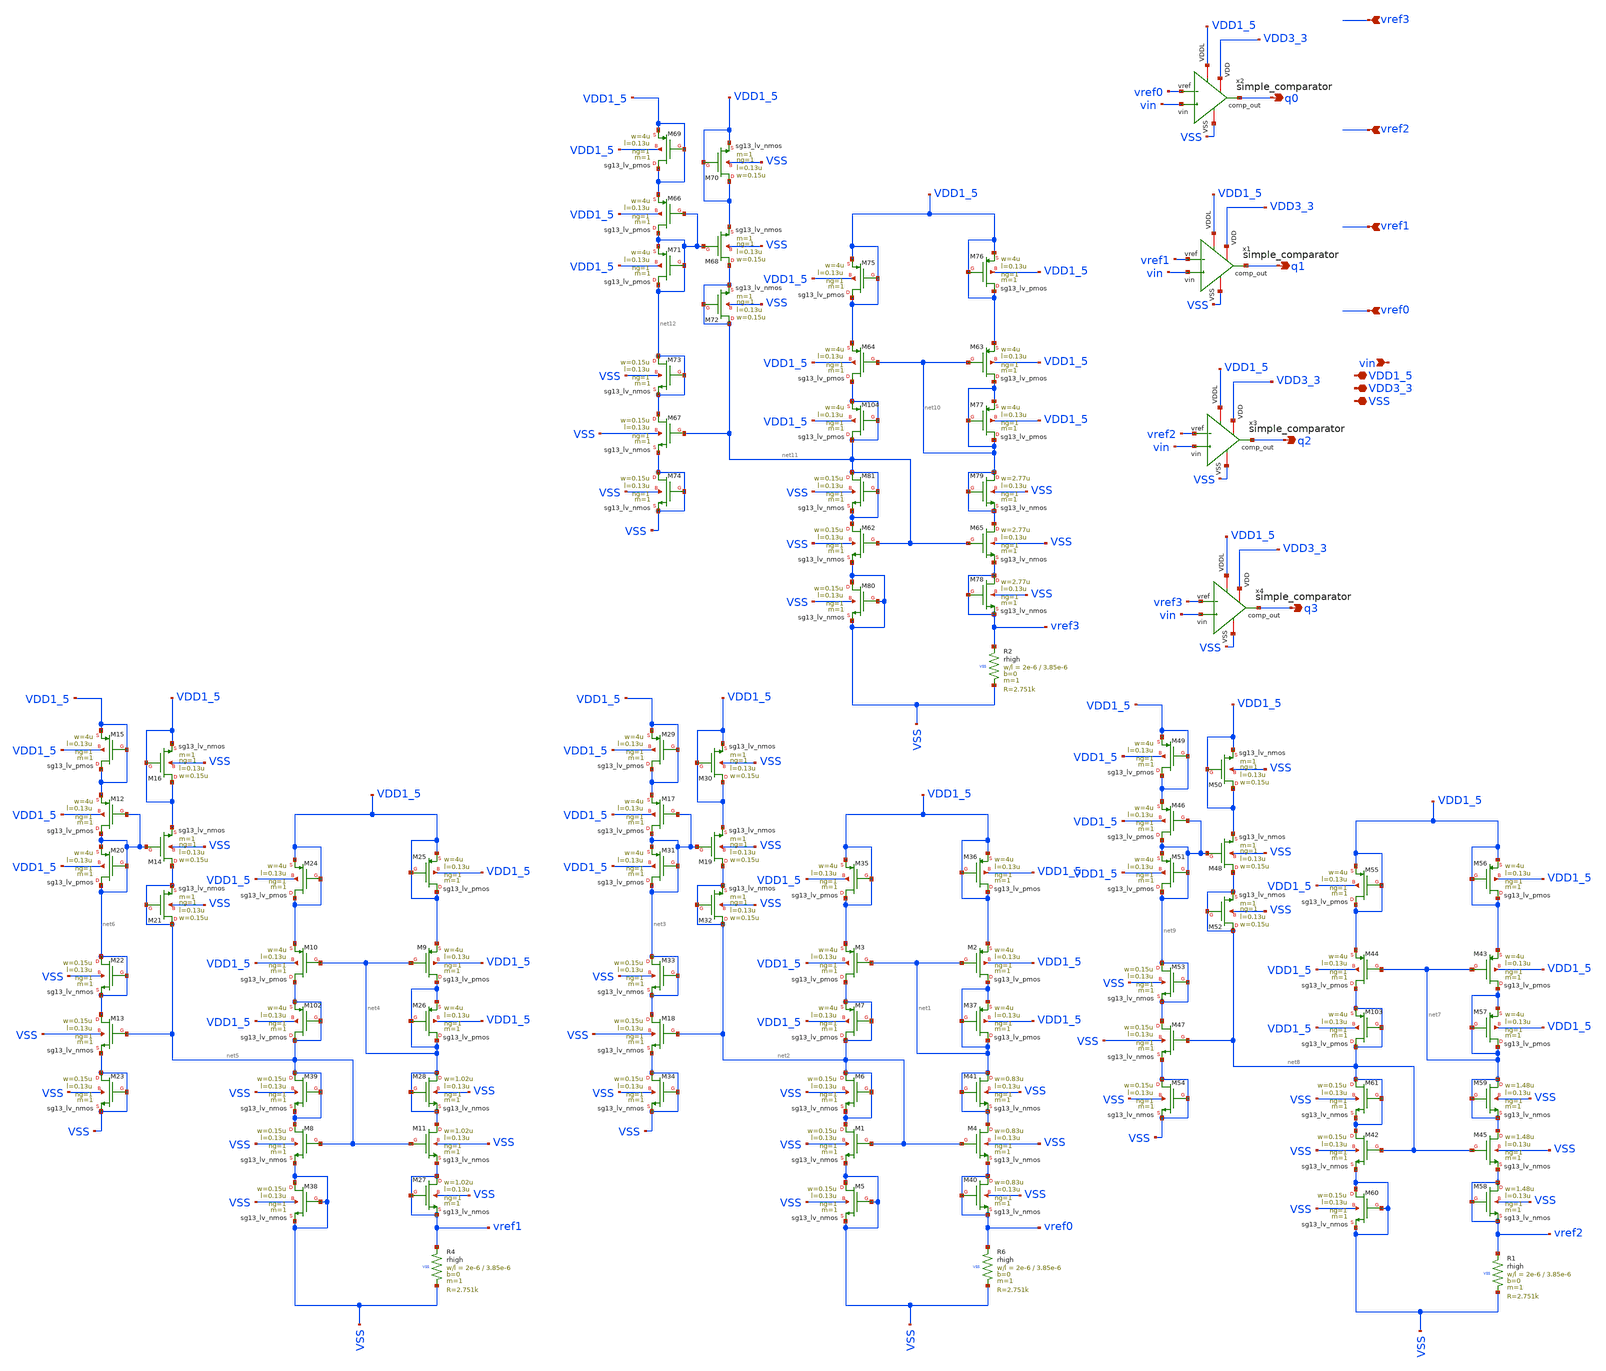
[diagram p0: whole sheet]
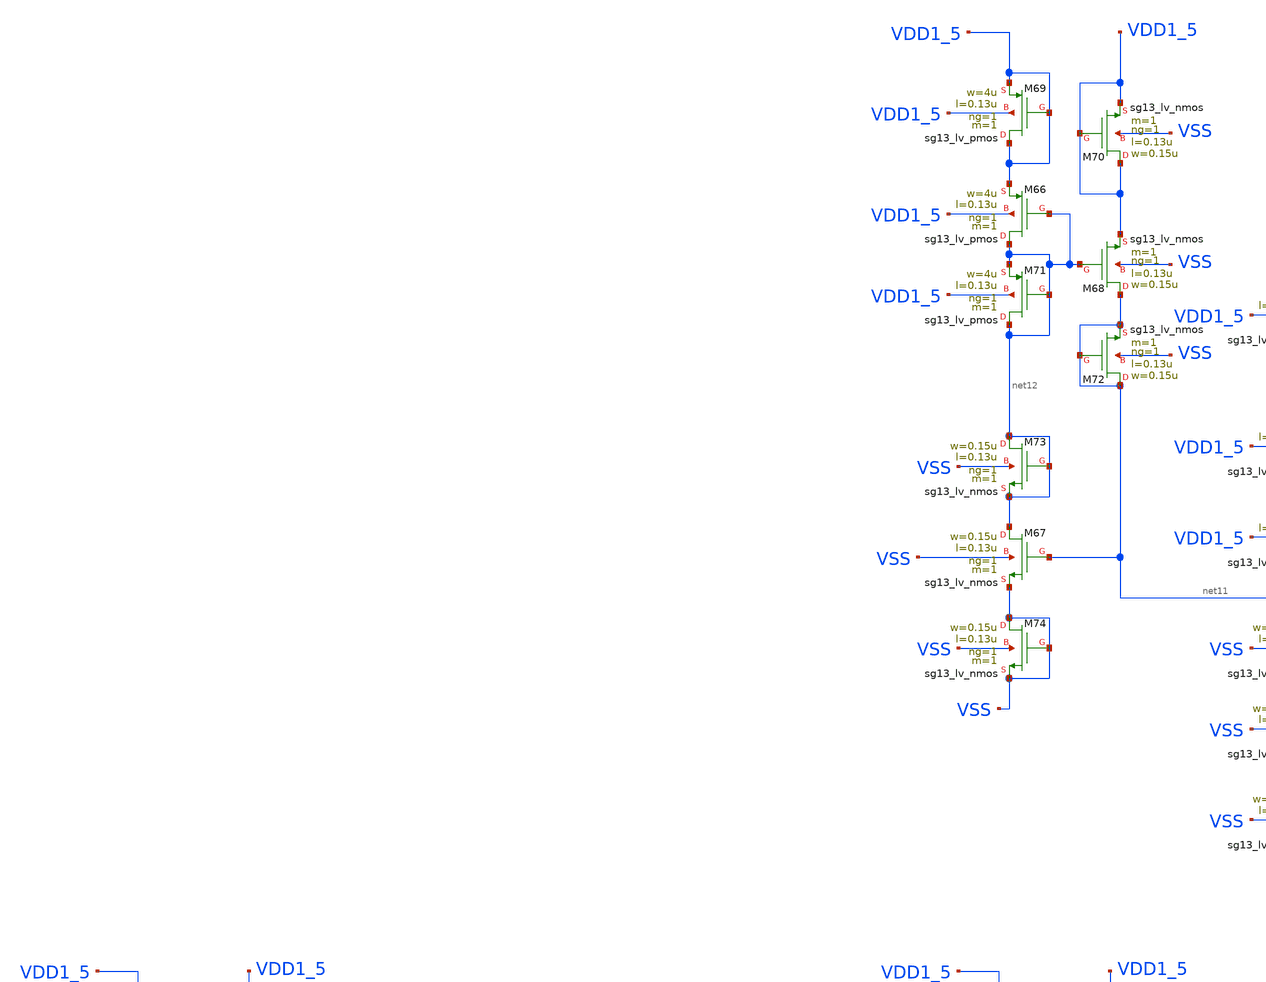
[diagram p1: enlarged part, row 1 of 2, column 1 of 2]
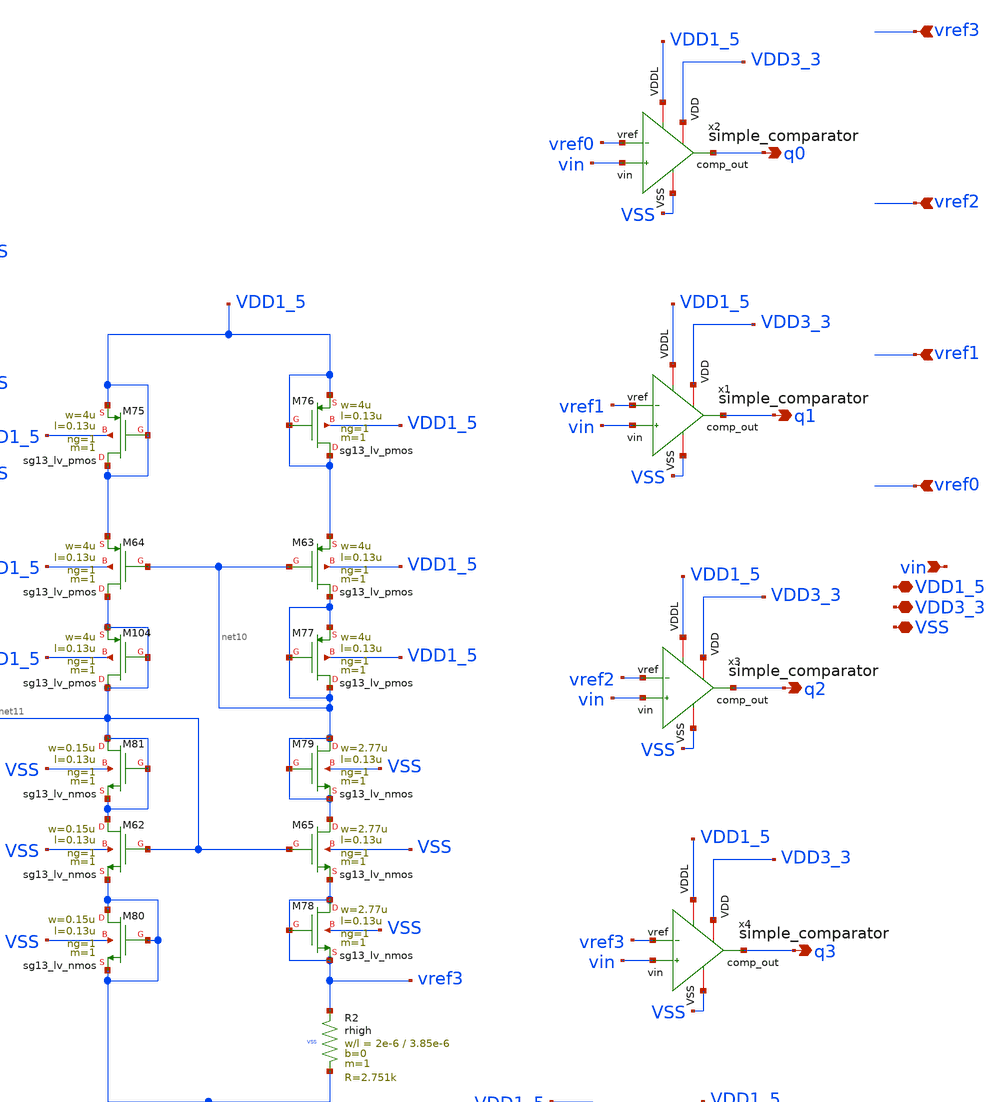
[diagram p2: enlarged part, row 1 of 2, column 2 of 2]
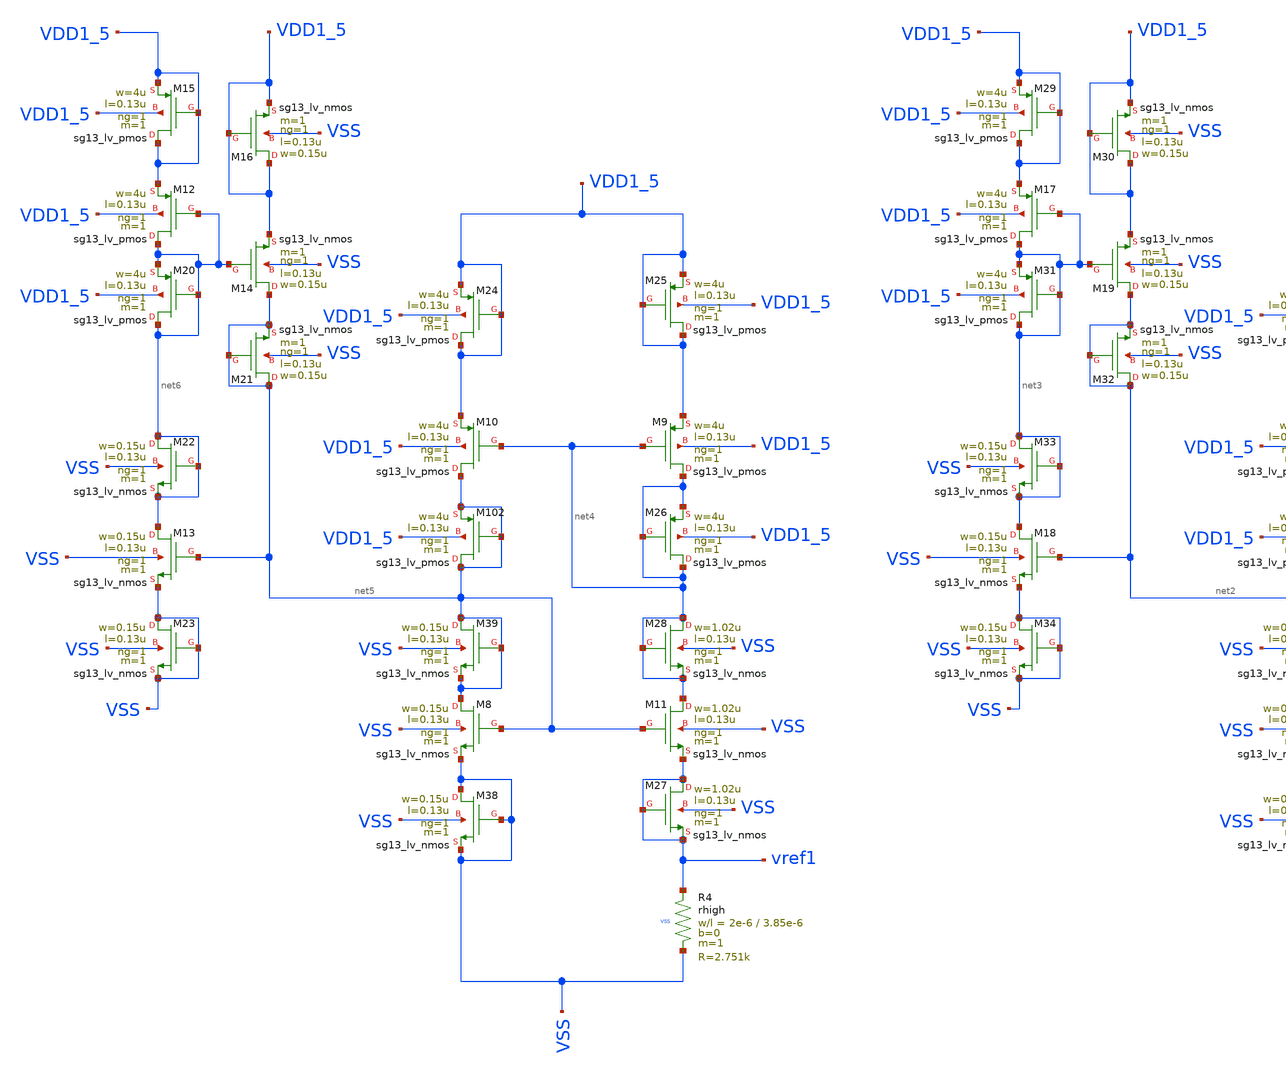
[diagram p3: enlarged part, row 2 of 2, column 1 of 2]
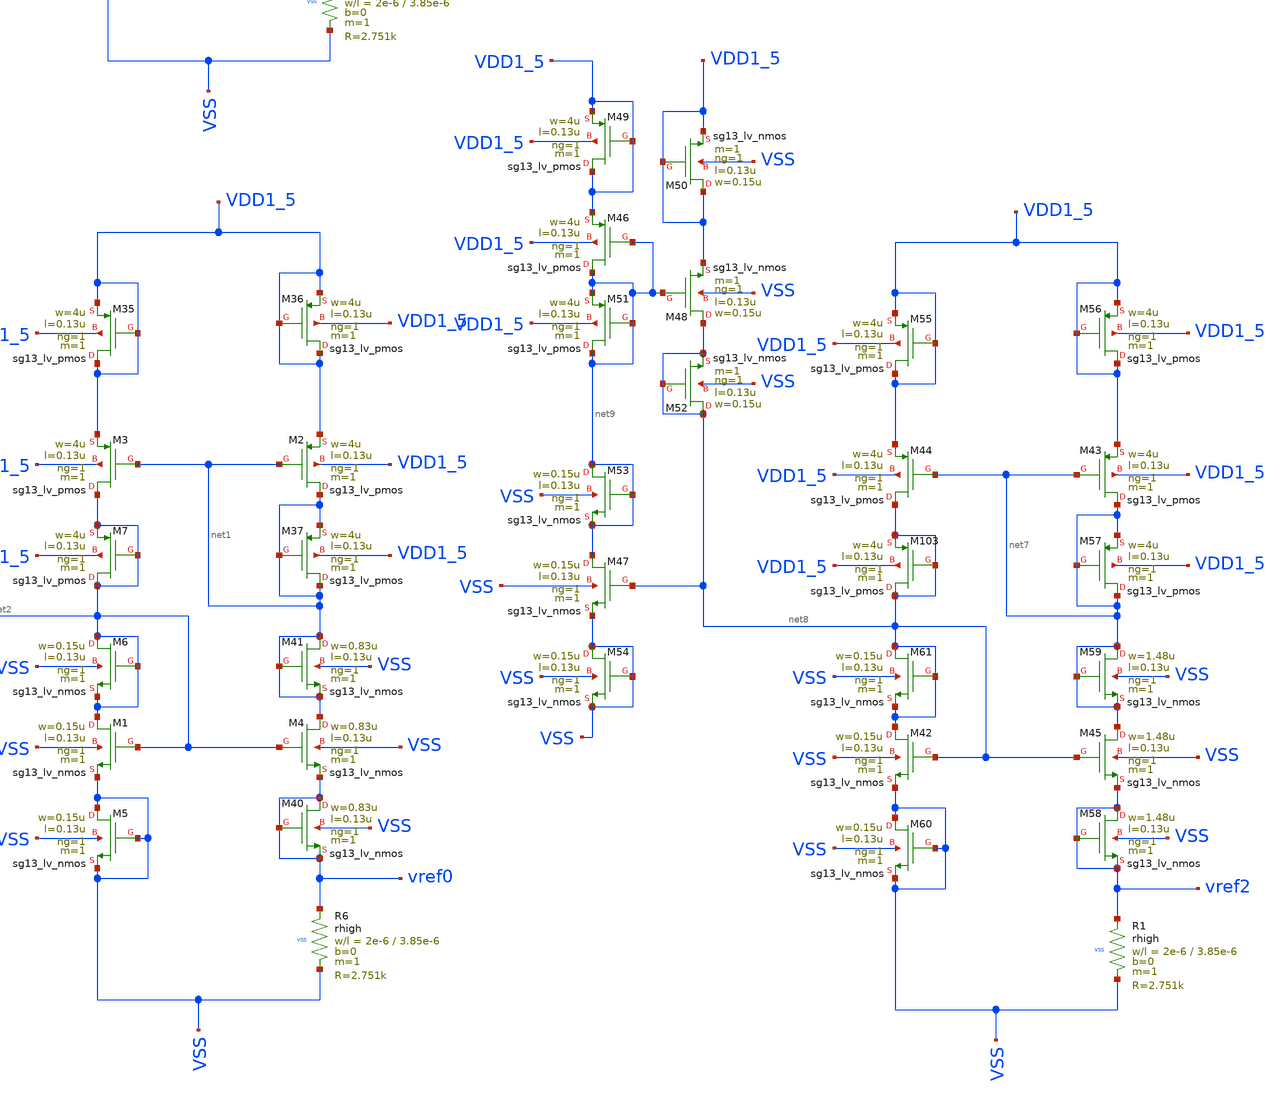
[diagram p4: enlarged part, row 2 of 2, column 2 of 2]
** sch_path: macros/heichips26_ook_top/macros/ook_analog_system/schematic/xschem/simple_comparator_stage.sch
**.subckt simple_comparator_stage VDD3_3 VSS VDD1_5 vin q0 vref3 vref2 vref1 vref0 q1 q2 q3
*.iopin VDD3_3
*.iopin VSS
*.iopin VDD1_5
*.ipin vin
*.opin q0
*.ipin vref3
*.ipin vref2
*.ipin vref1
*.ipin vref0
*.opin q1
*.opin q2
*.opin q3
x2 VDD1_5 VSS VDD3_3 vref0 vin q0 simple_comparator
x1 VDD1_5 VSS VDD3_3 vref1 vin q1 simple_comparator
x3 VDD1_5 VSS VDD3_3 vref2 vin q2 simple_comparator
x4 VDD1_5 VSS VDD3_3 vref3 vin q3 simple_comparator
XM1 net2 net2 VSS VSS sg13_lv_nmos w=0.15u l=0.13u ng=1 m=1 mm_ok=1
XM2 net1 net1 VDD1_5 VDD1_5 sg13_lv_pmos w=4u l=0.13u ng=1 m=1 mm_ok=1
XR6 vref0 VSS VSS rhigh w=2e-6 l=3.85e-6 m=1 b=0 mm_ok=1
XM3 net2 net1 VDD1_5 VDD1_5 sg13_lv_pmos w=4u l=0.13u ng=1 m=1 mm_ok=1
XM4 net1 net2 vref0 VSS sg13_lv_nmos w=0.83u l=0.13u ng=1 m=1 mm_ok=1
XM17 net3 net3 VDD1_5 VDD1_5 sg13_lv_pmos w=4u l=0.13u ng=1 m=1 mm_ok=1
XM18 net3 net2 VSS VSS sg13_lv_nmos w=0.15u l=0.13u ng=1 m=1 mm_ok=1
XM19 net2 net3 VDD1_5 VSS sg13_lv_nmos w=0.15u l=0.13u ng=1 m=1 mm_ok=1
XM29 VDD1_5 VDD1_5 VDD1_5 VDD1_5 sg13_lv_pmos w=4u l=0.13u ng=1 m=1 mm_ok=1
XM30 VDD1_5 VDD1_5 VDD1_5 VSS sg13_lv_nmos w=0.15u l=0.13u ng=1 m=1 mm_ok=1
XM31 net3 net3 net3 VDD1_5 sg13_lv_pmos w=4u l=0.13u ng=1 m=1 mm_ok=1
XM32 net2 net2 net2 VSS sg13_lv_nmos w=0.15u l=0.13u ng=1 m=1 mm_ok=1
XM33 net3 net3 net3 VSS sg13_lv_nmos w=0.15u l=0.13u ng=1 m=1 mm_ok=1
XM34 VSS VSS VSS VSS sg13_lv_nmos w=0.15u l=0.13u ng=1 m=1 mm_ok=1
XM35 VDD1_5 VDD1_5 VDD1_5 VDD1_5 sg13_lv_pmos w=4u l=0.13u ng=1 m=1 mm_ok=1
XM36 VDD1_5 VDD1_5 VDD1_5 VDD1_5 sg13_lv_pmos w=4u l=0.13u ng=1 m=1 mm_ok=1
XM37 net1 net1 net1 VDD1_5 sg13_lv_pmos w=4u l=0.13u ng=1 m=1 mm_ok=1
XM40 vref0 vref0 vref0 VSS sg13_lv_nmos w=0.83u l=0.13u ng=1 m=1 mm_ok=1
XM41 net1 net1 net1 VSS sg13_lv_nmos w=0.83u l=0.13u ng=1 m=1 mm_ok=1
XM5 VSS VSS VSS VSS sg13_lv_nmos w=0.15u l=0.13u ng=1 m=1 mm_ok=1
XM6 net2 net2 net2 VSS sg13_lv_nmos w=0.15u l=0.13u ng=1 m=1 mm_ok=1
XM7 net2 net2 net2 VDD1_5 sg13_lv_pmos w=4u l=0.13u ng=1 m=1 mm_ok=1
XM8 net5 net5 VSS VSS sg13_lv_nmos w=0.15u l=0.13u ng=1 m=1 mm_ok=1
XM9 net4 net4 VDD1_5 VDD1_5 sg13_lv_pmos w=4u l=0.13u ng=1 m=1 mm_ok=1
XR4 vref1 VSS VSS rhigh w=2e-6 l=3.85e-6 m=1 b=0 mm_ok=1
XM10 net5 net4 VDD1_5 VDD1_5 sg13_lv_pmos w=4u l=0.13u ng=1 m=1 mm_ok=1
XM11 net4 net5 vref1 VSS sg13_lv_nmos w=1.02u l=0.13u ng=1 m=1 mm_ok=1
XM12 net6 net6 VDD1_5 VDD1_5 sg13_lv_pmos w=4u l=0.13u ng=1 m=1 mm_ok=1
XM13 net6 net5 VSS VSS sg13_lv_nmos w=0.15u l=0.13u ng=1 m=1 mm_ok=1
XM14 net5 net6 VDD1_5 VSS sg13_lv_nmos w=0.15u l=0.13u ng=1 m=1 mm_ok=1
XM15 VDD1_5 VDD1_5 VDD1_5 VDD1_5 sg13_lv_pmos w=4u l=0.13u ng=1 m=1 mm_ok=1
XM16 VDD1_5 VDD1_5 VDD1_5 VSS sg13_lv_nmos w=0.15u l=0.13u ng=1 m=1 mm_ok=1
XM20 net6 net6 net6 VDD1_5 sg13_lv_pmos w=4u l=0.13u ng=1 m=1 mm_ok=1
XM21 net5 net5 net5 VSS sg13_lv_nmos w=0.15u l=0.13u ng=1 m=1 mm_ok=1
XM22 net6 net6 net6 VSS sg13_lv_nmos w=0.15u l=0.13u ng=1 m=1 mm_ok=1
XM23 VSS VSS VSS VSS sg13_lv_nmos w=0.15u l=0.13u ng=1 m=1 mm_ok=1
XM24 VDD1_5 VDD1_5 VDD1_5 VDD1_5 sg13_lv_pmos w=4u l=0.13u ng=1 m=1 mm_ok=1
XM25 VDD1_5 VDD1_5 VDD1_5 VDD1_5 sg13_lv_pmos w=4u l=0.13u ng=1 m=1 mm_ok=1
XM26 net4 net4 net4 VDD1_5 sg13_lv_pmos w=4u l=0.13u ng=1 m=1 mm_ok=1
XM27 vref1 vref1 vref1 VSS sg13_lv_nmos w=1.02u l=0.13u ng=1 m=1 mm_ok=1
XM28 net4 net4 net4 VSS sg13_lv_nmos w=1.02u l=0.13u ng=1 m=1 mm_ok=1
XM38 VSS VSS VSS VSS sg13_lv_nmos w=0.15u l=0.13u ng=1 m=1 mm_ok=1
XM39 net5 net5 net5 VSS sg13_lv_nmos w=0.15u l=0.13u ng=1 m=1 mm_ok=1
XM102 net5 net5 net5 VDD1_5 sg13_lv_pmos w=4u l=0.13u ng=1 m=1 mm_ok=1
XM42 net8 net8 VSS VSS sg13_lv_nmos w=0.15u l=0.13u ng=1 m=1 mm_ok=1
XM43 net7 net7 VDD1_5 VDD1_5 sg13_lv_pmos w=4u l=0.13u ng=1 m=1 mm_ok=1
XR1 vref2 VSS VSS rhigh w=2e-6 l=3.85e-6 m=1 b=0 mm_ok=1
XM44 net8 net7 VDD1_5 VDD1_5 sg13_lv_pmos w=4u l=0.13u ng=1 m=1 mm_ok=1
XM45 net7 net8 vref2 VSS sg13_lv_nmos w=1.48u l=0.13u ng=1 m=1 mm_ok=1
XM46 net9 net9 VDD1_5 VDD1_5 sg13_lv_pmos w=4u l=0.13u ng=1 m=1 mm_ok=1
XM47 net9 net8 VSS VSS sg13_lv_nmos w=0.15u l=0.13u ng=1 m=1 mm_ok=1
XM48 net8 net9 VDD1_5 VSS sg13_lv_nmos w=0.15u l=0.13u ng=1 m=1 mm_ok=1
XM49 VDD1_5 VDD1_5 VDD1_5 VDD1_5 sg13_lv_pmos w=4u l=0.13u ng=1 m=1 mm_ok=1
XM50 VDD1_5 VDD1_5 VDD1_5 VSS sg13_lv_nmos w=0.15u l=0.13u ng=1 m=1 mm_ok=1
XM51 net9 net9 net9 VDD1_5 sg13_lv_pmos w=4u l=0.13u ng=1 m=1 mm_ok=1
XM52 net8 net8 net8 VSS sg13_lv_nmos w=0.15u l=0.13u ng=1 m=1 mm_ok=1
XM53 net9 net9 net9 VSS sg13_lv_nmos w=0.15u l=0.13u ng=1 m=1 mm_ok=1
XM54 VSS VSS VSS VSS sg13_lv_nmos w=0.15u l=0.13u ng=1 m=1 mm_ok=1
XM55 VDD1_5 VDD1_5 VDD1_5 VDD1_5 sg13_lv_pmos w=4u l=0.13u ng=1 m=1 mm_ok=1
XM56 VDD1_5 VDD1_5 VDD1_5 VDD1_5 sg13_lv_pmos w=4u l=0.13u ng=1 m=1 mm_ok=1
XM57 net7 net7 net7 VDD1_5 sg13_lv_pmos w=4u l=0.13u ng=1 m=1 mm_ok=1
XM58 vref2 vref2 vref2 VSS sg13_lv_nmos w=1.48u l=0.13u ng=1 m=1 mm_ok=1
XM59 net7 net7 net7 VSS sg13_lv_nmos w=1.48u l=0.13u ng=1 m=1 mm_ok=1
XM60 VSS VSS VSS VSS sg13_lv_nmos w=0.15u l=0.13u ng=1 m=1 mm_ok=1
XM61 net8 net8 net8 VSS sg13_lv_nmos w=0.15u l=0.13u ng=1 m=1 mm_ok=1
XM103 net8 net8 net8 VDD1_5 sg13_lv_pmos w=4u l=0.13u ng=1 m=1 mm_ok=1
XM62 net11 net11 VSS VSS sg13_lv_nmos w=0.15u l=0.13u ng=1 m=1 mm_ok=1
XM63 net10 net10 VDD1_5 VDD1_5 sg13_lv_pmos w=4u l=0.13u ng=1 m=1 mm_ok=1
XR2 vref3 VSS VSS rhigh w=2e-6 l=3.85e-6 m=1 b=0 mm_ok=1
XM64 net11 net10 VDD1_5 VDD1_5 sg13_lv_pmos w=4u l=0.13u ng=1 m=1 mm_ok=1
XM65 net10 net11 vref3 VSS sg13_lv_nmos w=2.77u l=0.13u ng=1 m=1 mm_ok=1
XM66 net12 net12 VDD1_5 VDD1_5 sg13_lv_pmos w=4u l=0.13u ng=1 m=1 mm_ok=1
XM67 net12 net11 VSS VSS sg13_lv_nmos w=0.15u l=0.13u ng=1 m=1 mm_ok=1
XM68 net11 net12 VDD1_5 VSS sg13_lv_nmos w=0.15u l=0.13u ng=1 m=1 mm_ok=1
XM69 VDD1_5 VDD1_5 VDD1_5 VDD1_5 sg13_lv_pmos w=4u l=0.13u ng=1 m=1 mm_ok=1
XM70 VDD1_5 VDD1_5 VDD1_5 VSS sg13_lv_nmos w=0.15u l=0.13u ng=1 m=1 mm_ok=1
XM71 net12 net12 net12 VDD1_5 sg13_lv_pmos w=4u l=0.13u ng=1 m=1 mm_ok=1
XM72 net11 net11 net11 VSS sg13_lv_nmos w=0.15u l=0.13u ng=1 m=1 mm_ok=1
XM73 net12 net12 net12 VSS sg13_lv_nmos w=0.15u l=0.13u ng=1 m=1 mm_ok=1
XM74 VSS VSS VSS VSS sg13_lv_nmos w=0.15u l=0.13u ng=1 m=1 mm_ok=1
XM75 VDD1_5 VDD1_5 VDD1_5 VDD1_5 sg13_lv_pmos w=4u l=0.13u ng=1 m=1 mm_ok=1
XM76 VDD1_5 VDD1_5 VDD1_5 VDD1_5 sg13_lv_pmos w=4u l=0.13u ng=1 m=1 mm_ok=1
XM77 net10 net10 net10 VDD1_5 sg13_lv_pmos w=4u l=0.13u ng=1 m=1 mm_ok=1
XM78 vref3 vref3 vref3 VSS sg13_lv_nmos w=2.77u l=0.13u ng=1 m=1 mm_ok=1
XM79 net10 net10 net10 VSS sg13_lv_nmos w=2.77u l=0.13u ng=1 m=1 mm_ok=1
XM80 VSS VSS VSS VSS sg13_lv_nmos w=0.15u l=0.13u ng=1 m=1 mm_ok=1
XM81 net11 net11 net11 VSS sg13_lv_nmos w=0.15u l=0.13u ng=1 m=1 mm_ok=1
XM104 net11 net11 net11 VDD1_5 sg13_lv_pmos w=4u l=0.13u ng=1 m=1 mm_ok=1
**.ends

* expanding   symbol:  simple_comparator.sym # of pins=6
** sym_path: macros/heichips26_ook_top/macros/ook_analog_system/schematic/xschem/simple_comparator.sym
** sch_path: macros/heichips26_ook_top/macros/ook_analog_system/schematic/xschem/simple_comparator.sch
.subckt simple_comparator VDDL VSS VDD vref vin comp_out
*.ipin vin
*.ipin vref
*.iopin VDD
*.iopin VSS
*.opin comp_out
*.iopin VDDL
XMBIAS vbias vbias VDD VDD sg13_hv_pmos w=4u l=0.5u ng=1 m=1 mm_ok=1
XRBIAS vbias VSS VSS rhigh w=2e-6 l=9.27e-6 m=1 b=15 ps=0.18e-6 mm_ok=1
XM3P net4 vbias VDD VDD sg13_hv_pmos w=4u l=0.5u ng=1 m=1 mm_ok=1
XM1P outn vin net4 VDD sg13_hv_pmos w=4u l=0.5u ng=1 m=4 mm_ok=1
XM2P net1 vref net4 VDD sg13_hv_pmos w=4u l=0.5u ng=1 m=4 mm_ok=1
XM4N outn outn VSS VSS sg13_hv_nmos w=2u l=0.5u ng=1 m=4 mm_ok=1
XM5N net1 outn VSS VSS sg13_hv_nmos w=2u l=0.5u ng=1 m=4 mm_ok=1
XMP1 net2 net1 VDD VDD sg13_hv_pmos w=8u l=0.45u ng=1 m=1 mm_ok=1
XMN1 net2 net1 VSS VSS sg13_hv_nmos w=4u l=0.45u ng=1 m=1 mm_ok=1
XMP2 comp_out net3 VDDL VDDL sg13_lv_pmos w=8u l=0.13u ng=1 m=1 mm_ok=1
XMBIAS1 vbias vbias vbias VDD sg13_hv_pmos w=4u l=0.5u ng=1 m=1 mm_ok=1
XMBIAS2 VDD VDD VDD VDD sg13_hv_pmos w=4u l=0.5u ng=1 m=1 mm_ok=1
XM1 VDD VDD VDD VDD sg13_hv_pmos w=4u l=0.5u ng=1 m=1 mm_ok=1
XM2 net4 net4 net4 VDD sg13_hv_pmos w=4u l=0.5u ng=1 m=1 mm_ok=1
XMP3 net2 net2 net2 VDD sg13_hv_pmos w=8u l=0.45u ng=1 m=1 mm_ok=1
XMP4 VDD VDD VDD VDD sg13_hv_pmos w=8u l=0.45u ng=1 m=1 mm_ok=1
XMP5 VDDL VDDL VDDL VDDL sg13_lv_pmos w=8u l=0.13u ng=1 m=1 mm_ok=1
XMP6 comp_out comp_out comp_out VDDL sg13_lv_pmos w=8u l=0.13u ng=1 m=1 mm_ok=1
XMN3 comp_out comp_out comp_out VSS sg13_lv_nmos w=4u l=0.13u ng=1 m=1 mm_ok=1
XMN4 VSS VSS VSS VSS sg13_lv_nmos w=4u l=0.13u ng=1 m=1 mm_ok=1
XMN5 net2 net2 net2 VSS sg13_hv_nmos w=4u l=0.45u ng=1 m=1 mm_ok=1
XMN6 VSS VSS VSS VSS sg13_hv_nmos w=4u l=0.45u ng=1 m=1 mm_ok=1
XM3 net4 net4 net4 VDD sg13_hv_pmos w=4u l=0.5u ng=1 m=1 mm_ok=1
XM4 outn outn outn VDD sg13_hv_pmos w=4u l=0.5u ng=1 m=1 mm_ok=1
XM5 net1 net1 net1 VSS sg13_hv_nmos w=2u l=0.5u ng=1 m=1 mm_ok=1
XM6 VSS VSS VSS VSS sg13_hv_nmos w=2u l=0.5u ng=1 m=1 mm_ok=1
XM7 net4 net4 net4 VDD sg13_hv_pmos w=4u l=0.5u ng=1 m=1 mm_ok=1
XM8 net1 net1 net1 VDD sg13_hv_pmos w=4u l=0.5u ng=1 m=1 mm_ok=1
XM9 outn outn outn VSS sg13_hv_nmos w=2u l=0.5u ng=1 m=1 mm_ok=1
XM10 VSS VSS VSS VSS sg13_hv_nmos w=2u l=0.5u ng=1 m=1 mm_ok=1
XMN8 comp_out net3 VSS VSS sg13_lv_nmos w=4u l=0.13u ng=1 m=1 mm_ok=1
XMP7 net3 net2 VDDL VDDL sg13_hv_pmos w=8u l=0.45u ng=1 m=1 mm_ok=1
XMN2 net3 net2 VSS VSS sg13_hv_nmos w=4u l=0.45u ng=1 m=1 mm_ok=1
XMP8 net3 net3 net3 VDDL sg13_hv_pmos w=8u l=0.45u ng=1 m=1 mm_ok=1
XMP9 VDDL VDDL VDDL VDDL sg13_hv_pmos w=8u l=0.45u ng=1 m=1 mm_ok=1
XMN7 net3 net3 net3 VSS sg13_hv_nmos w=4u l=0.45u ng=1 m=1 mm_ok=1
XMN9 VSS VSS VSS VSS sg13_hv_nmos w=4u l=0.45u ng=1 m=1 mm_ok=1
.ends

.end
